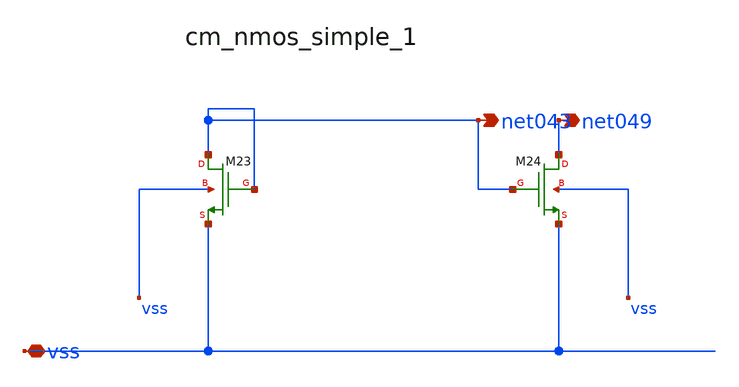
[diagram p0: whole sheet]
** sch_path: analog-db/raw/amp_007_leung_dfcfc2/hier/blocks/cm_nmos_simple_1.sch
**.subckt cm_nmos_simple_1 vss net043 net049
*.iopin vss
*.opin net043
*.opin net049
XM23 net043 net043 vss vss sg13_lv_nmos w=x_dut_xm23_w l=x_dut_xm23_l ng=1 m=x_dut_xm23_m
XM24 net049 net043 vss vss sg13_lv_nmos w=x_dut_xm24_w l=x_dut_xm24_l ng=1 m=x_dut_xm24_m
**.ends
.end
